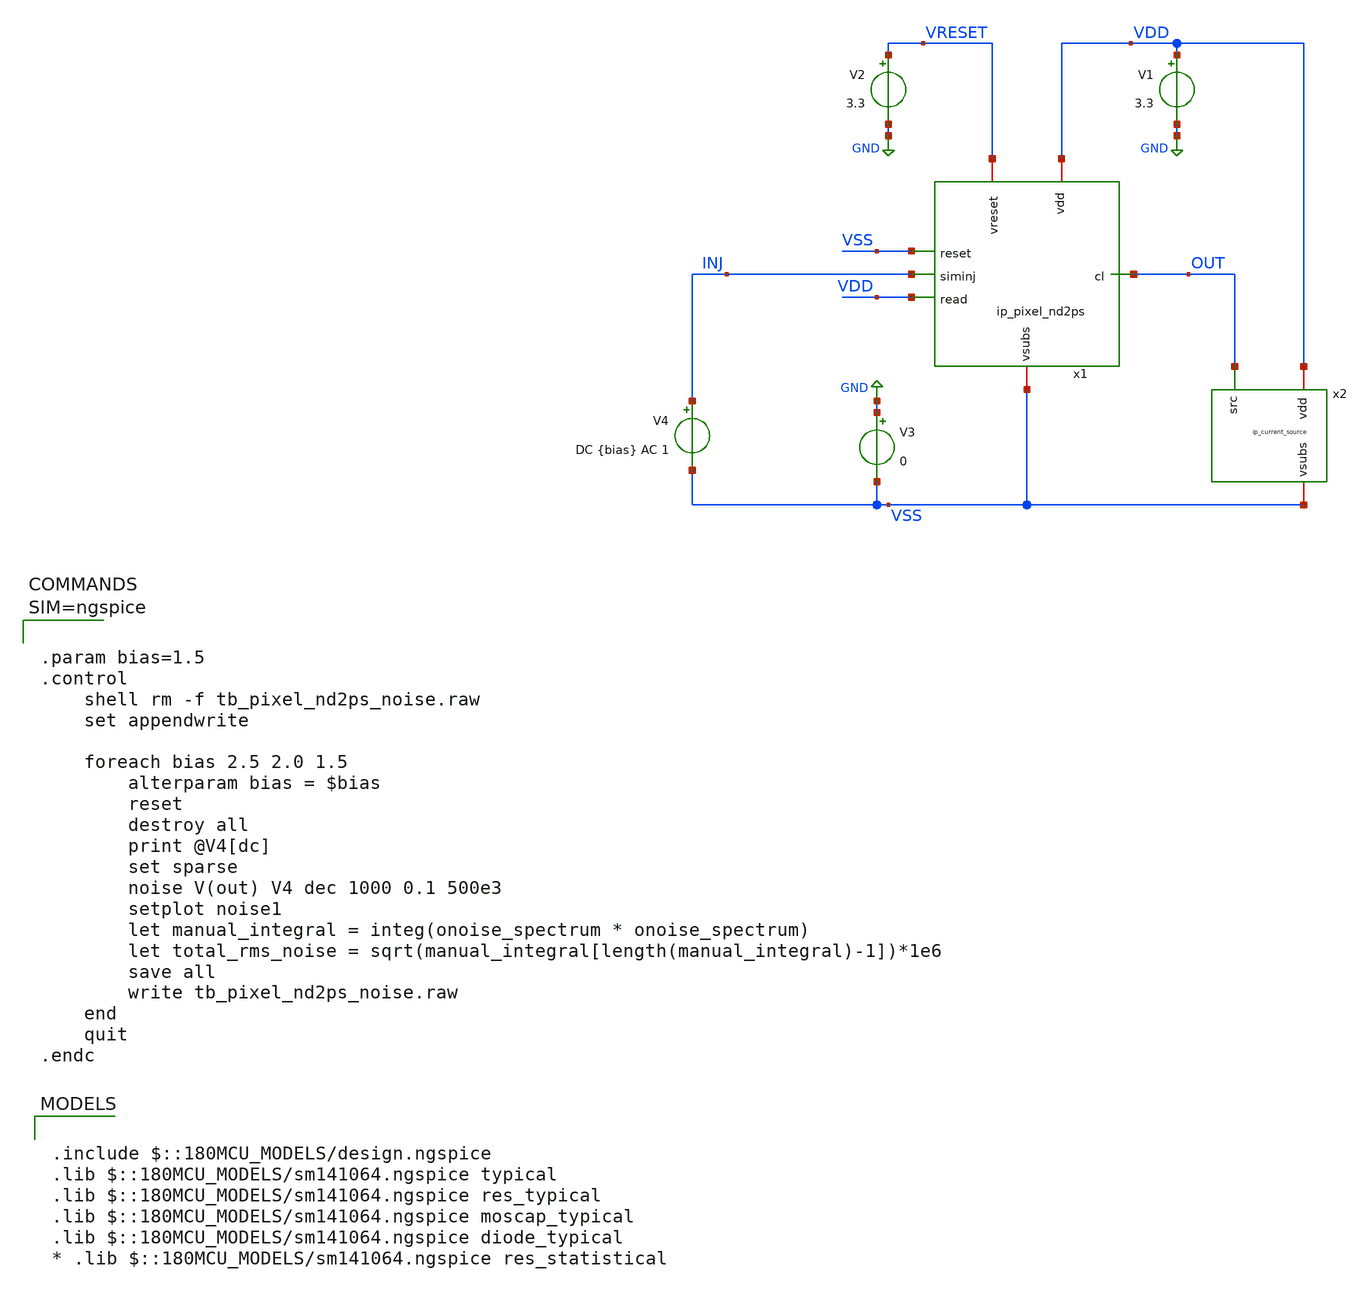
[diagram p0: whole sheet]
** sch_path: xschem/tb_pixel_nd2ps_noise.sch
**.subckt tb_pixel_nd2ps_noise
V1 VDD GND 3.3
V2 VRESET GND 3.3
V3 GND VSS 0
x1 VDD VRESET VSS INJ OUT VDD VSS ip_pixel_nd2ps
V4 INJ VSS DC {bias} AC 1
x2 VDD OUT VSS ip_current_source
**** begin user architecture code

.include $::180MCU_MODELS/design.ngspice
.lib $::180MCU_MODELS/sm141064.ngspice typical
.lib $::180MCU_MODELS/sm141064.ngspice res_typical
.lib $::180MCU_MODELS/sm141064.ngspice moscap_typical
.lib $::180MCU_MODELS/sm141064.ngspice diode_typical
* .lib $::180MCU_MODELS/sm141064.ngspice res_statistical




.param bias=1.5
.control
	shell rm -f tb_pixel_nd2ps_noise.raw
	set appendwrite

	foreach bias 2.5 2.0 1.5
		alterparam bias = $bias
		reset
		destroy all
		print @V4[dc]
		set sparse
		noise V(out) V4 dec 1000 0.1 500e3
		setplot noise1
		let manual_integral = integ(onoise_spectrum * onoise_spectrum)
		let total_rms_noise = sqrt(manual_integral[length(manual_integral)-1])*1e6
		save all
		write tb_pixel_nd2ps_noise.raw
	end
	quit
.endc



**** end user architecture code
**.ends

* expanding   symbol:  ip_pixel_nd2ps.sym # of pins=7
** sym_path: xschem/ip_pixel_nd2ps.sym
** sch_path: xschem/ip_pixel_nd2ps.sch
.subckt ip_pixel_nd2ps vdd vreset reset siminj cl read vsubs
*.iopin vdd
*.iopin vsubs
*.ipin siminj
*.ipin reset
*.ipin read
*.iopin vreset
*.opin cl
XM1 vreset reset siminj vsubs nfet_03v3 L=0.3u W=0.3u nf=1 ad='int((nf+1)/2) * W/nf * 0.18u' as='int((nf+2)/2) * W/nf * 0.18u'
+ pd='2*int((nf+1)/2) * (W/nf + 0.18u)' ps='2*int((nf+2)/2) * (W/nf + 0.18u)' nrd='0.18u / W' nrs='0.18u / W'
+ sa=0 sb=0 sd=0 m=1
XM2 vdd siminj sfout vsubs nfet_03v3 L=0.3u W=0.3u nf=1 ad='int((nf+1)/2) * W/nf * 0.18u' as='int((nf+2)/2) * W/nf * 0.18u'
+ pd='2*int((nf+1)/2) * (W/nf + 0.18u)' ps='2*int((nf+2)/2) * (W/nf + 0.18u)' nrd='0.18u / W' nrs='0.18u / W'
+ sa=0 sb=0 sd=0 m=1
XM3 sfout read cl vsubs nfet_03v3 L=0.3u W=1u nf=1 ad='int((nf+1)/2) * W/nf * 0.18u' as='int((nf+2)/2) * W/nf * 0.18u'
+ pd='2*int((nf+1)/2) * (W/nf + 0.18u)' ps='2*int((nf+2)/2) * (W/nf + 0.18u)' nrd='0.18u / W' nrs='0.18u / W'
+ sa=0 sb=0 sd=0 m=1
D1 vsubs siminj diode_nd2ps_03v3 area='12u * 10u ' pj='2*12u + 2*10u ' m=1
.ends


* expanding   symbol:  ip_current_source.sym # of pins=3
** sym_path: xschem/ip_current_source.sym
** sch_path: xschem/ip_current_source.sch
.subckt ip_current_source vdd src vsubs
*.iopin vdd
*.iopin vsubs
*.ipin src
XM1 net1 net1 vsubs vsubs nfet_03v3 L=1u W=3u nf=1 ad='int((nf+1)/2) * W/nf * 0.18u' as='int((nf+2)/2) * W/nf * 0.18u'
+ pd='2*int((nf+1)/2) * (W/nf + 0.18u)' ps='2*int((nf+2)/2) * (W/nf + 0.18u)' nrd='0.18u / W' nrs='0.18u / W'
+ sa=0 sb=0 sd=0 m=1
XM2 net2 net1 vsubs vsubs nfet_03v3 L=10u W=0.3u nf=1 ad='int((nf+1)/2) * W/nf * 0.18u' as='int((nf+2)/2) * W/nf * 0.18u'
+ pd='2*int((nf+1)/2) * (W/nf + 0.18u)' ps='2*int((nf+2)/2) * (W/nf + 0.18u)' nrd='0.18u / W' nrs='0.18u / W'
+ sa=0 sb=0 sd=0 m=1
XR2 vdd net1 vsubs ppolyf_u_3k r_width=1e-6 r_length=6e-6 m=1
XM3 src net1 net2 vsubs nfet_03v3 L=0.3u W=10u nf=1 ad='int((nf+1)/2) * W/nf * 0.18u' as='int((nf+2)/2) * W/nf * 0.18u'
+ pd='2*int((nf+1)/2) * (W/nf + 0.18u)' ps='2*int((nf+2)/2) * (W/nf + 0.18u)' nrd='0.18u / W' nrs='0.18u / W'
+ sa=0 sb=0 sd=0 m=1
.ends

.GLOBAL GND
.end
